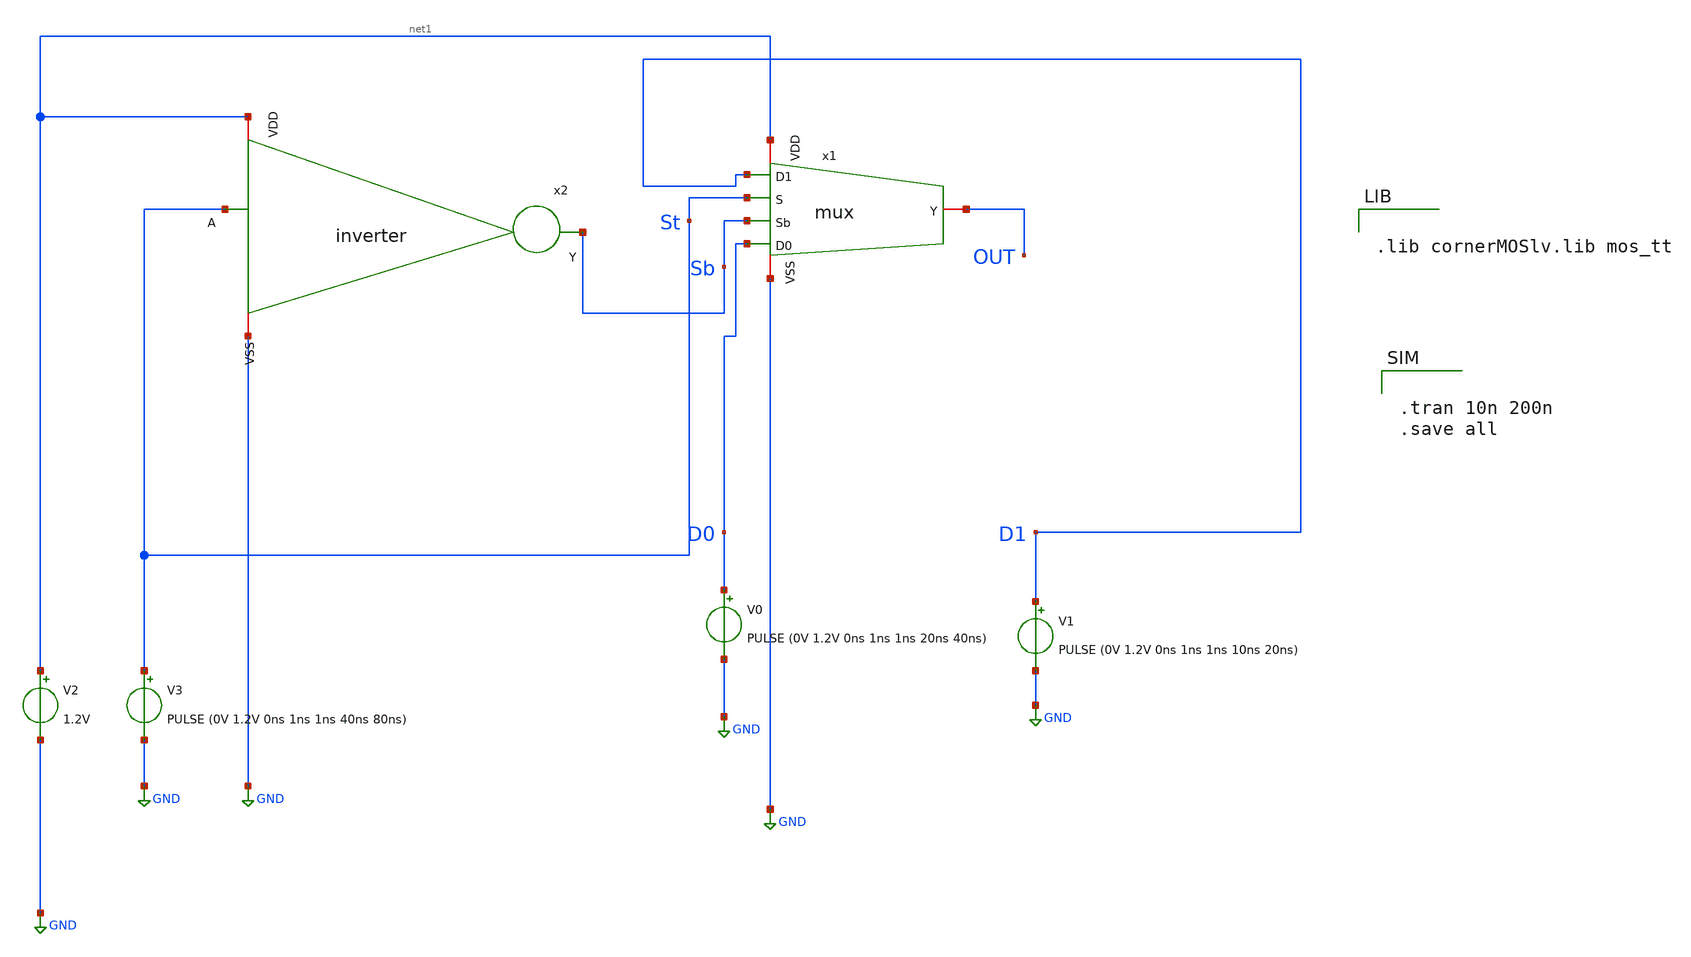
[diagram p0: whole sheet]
** sch_path: mux_testbench.sch
**.subckt mux_testbench
x1 net1 D1 OUT St Sb GND D0 mux
V2 net1 GND 1.2V
x2 net1 St Sb GND inverter
V0 D0 GND PULSE (0V 1.2V 0ns 1ns 1ns 20ns 40ns)
V1 D1 GND PULSE (0V 1.2V 0ns 1ns 1ns 10ns 20ns)
V3 St GND PULSE (0V 1.2V 0ns 1ns 1ns 40ns 80ns)
**** begin user architecture code


.tran 10n 200n
.save all




.lib cornerMOSlv.lib mos_tt

**** end user architecture code
**.ends

* expanding   symbol:  xchem/xchem/mux.sym # of pins=7
** sym_path: mux.sym
** sch_path: mux.sch
.subckt mux VDD D1 Y S Sb VSS D0
*.ipin S
*.ipin Sb
*.ipin D0
*.ipin D1
*.iopin VDD
*.iopin VSS
*.iopin Y
XM1 Y Sb D1 VDD sg13_lv_pmos w=0.15u l=0.13u ng=1 m=1 mm_ok=1
XM2 D0 S Y VDD sg13_lv_pmos w=0.15u l=0.13u ng=1 m=1 mm_ok=1
XM3 Y S D1 VSS sg13_lv_nmos w=0.15u l=0.13u ng=1 m=1 mm_ok=1
XM4 D0 Sb Y VSS sg13_lv_nmos w=0.15u l=0.13u ng=1 m=1 mm_ok=1
.ends


* expanding   symbol:  xchem/xchem/inverter.sym # of pins=4
** sym_path: inverter.sym
** sch_path: inverter.sch
.subckt inverter VDD A Y VSS
*.ipin A
*.iopin VDD
*.iopin VSS
*.opin Y
XM1 Y A VDD VDD sg13_lv_pmos w=0.15u l=0.13u ng=1 m=1 mm_ok=1
XM2 Y A VSS VSS sg13_lv_nmos w=0.15u l=0.13u ng=1 m=1 mm_ok=1
.ends

.GLOBAL GND
.end
